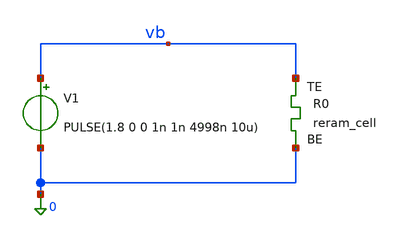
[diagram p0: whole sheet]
** sch_path: rram_test/1R.sch
**.subckt 1R
V1 vb 0 PULSE(1.8 0 0 1n 1n 4998n 10u)
XR0 vb 0 sky130_fd_pr_reram__reram_cell Tfilament_0=3.3e-9
**** begin user architecture code

** opencircuitdesign pdks install
.inc $::SKYWATER_MODELS/sky130_fd_pr_reram__reram_cell.spice



.tran 50n 310u
.control
	savecurrents
	save all
	run
	write 1R.raw
.endc



**** end user architecture code
**.ends
.end
